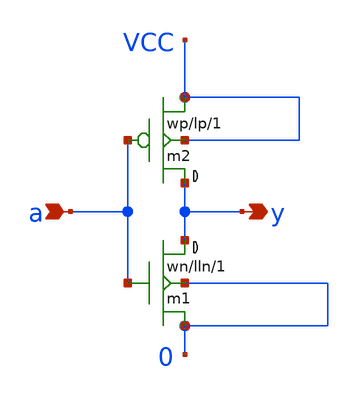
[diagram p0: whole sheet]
** sch_path: xschem-src/xschem_library/generators/my_inv.sch
* Copyright (C) 1998-2026 Stefan Frederik Schippers
* This program is free software; you can redistribute it and/or modify
* it under the terms of the GNU General Public License as published by
* the Free Software Foundation; either version 2 of the License, or
* (at your option) any later version.
* This program is distributed in the hope that it will be useful,
* but WITHOUT ANY WARRANTY; without even the implied warranty of
* MERCHANTABILITY or FITNESS FOR A PARTICULAR PURPOSE.  See the
* GNU General Public License for more details.
* You should have received a copy of the GNU General Public License
* along with this program; if not, write to the Free Software
**.subckt my_inv y a
*.opin y
*.ipin a
m2 y a VCC VCC cmosp w=wp l=lp ad='wp *4.6u' as='wp *4.6u' pd='wp *2+9.2u' ps='wp *2+9.2u' m=1
m1 y a 0 0 cmosn w=wn l=lln ad='wn *4.3u' as='wn *4.3u' pd='wn *2+8.6u' ps='wn *2+8.6u' m=1
**.ends
.end
